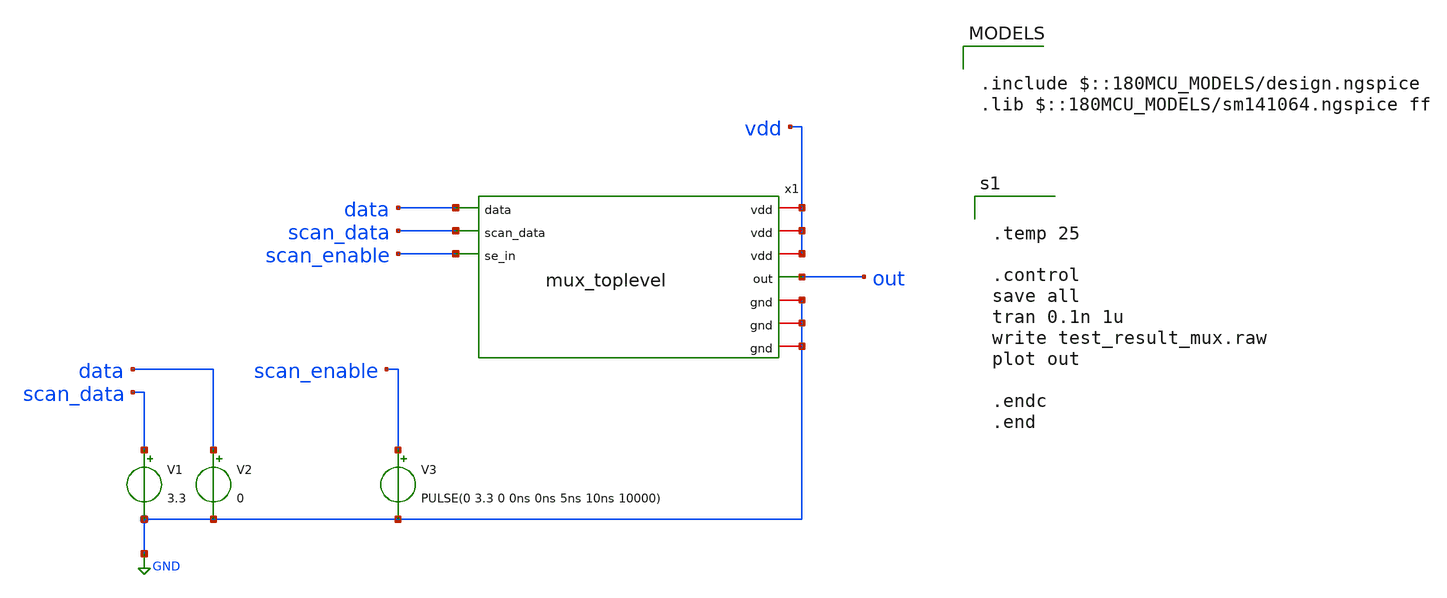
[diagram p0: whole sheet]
** sch_path: designs/schematics/mux2x1_transmission_gate/mux_tb.sch
**.subckt mux_tb
V1 scan_data GND 3.3
V2 data GND 0
V3 scan_enable GND PULSE(0 3.3 0 0ns 0ns 5ns 10ns 10000)
x1 vdd data GND out scan_data scan_enable mux_toplevel
**** begin user architecture code

.include $::180MCU_MODELS/design.ngspice
.lib $::180MCU_MODELS/sm141064.ngspice ff



.temp 25

.control
save all
tran 0.1n 1u
write test_result_mux.raw
plot out

.endc
.end


.option
save all

.control
tran 0 1u
.endc
.end
**** end user architecture code
**.ends

* expanding   symbol:  schematics/mux2x1_transmission_gate/mux_toplevel.sym # of pins=10
** sym_path: designs/schematics/mux2x1_transmission_gate/mux_toplevel.sym
** sch_path: designs/schematics/mux2x1_transmission_gate/mux_toplevel.sch
.subckt mux_toplevel vdd data gnd out scan_data se_in
*.iopin vdd
*.iopin gnd
*.opin out
*.ipin data
*.ipin scan_data
*.ipin se_in
*.iopin vdd
*.iopin gnd
*.iopin gnd
*.iopin vdd
x1 vdd se_in net1 gnd mux_ctrl_logic
x2 vdd net1 data out se_in gnd mux_tg
x3 vdd se_in scan_data out net1 gnd mux_tg
.ends


* expanding   symbol:  mux_transmission_gate/mux_ctrl_logic.sym # of pins=4
** sym_path: designs/schematics/mux2x1_transmission_gate/mux_ctrl_logic.sym
** sch_path: designs/schematics/mux2x1_transmission_gate/mux_ctrl_logic.sch
.subckt mux_ctrl_logic vdd in out_inv gnd
*.iopin vdd
*.iopin gnd
*.iopin out_inv
*.iopin in
XM1 out_inv in gnd gnd nfet_03v3 L=0.28u W=0.22u nf=1 ad='int((nf+1)/2) * W/nf * 0.18u' as='int((nf+2)/2) * W/nf * 0.18u'
+ pd='2*int((nf+1)/2) * (W/nf + 0.18u)' ps='2*int((nf+2)/2) * (W/nf + 0.18u)' nrd='0.18u / W' nrs='0.18u / W'
+ sa=0 sb=0 sd=0 m=1
XM2 out_inv in vdd vdd pfet_03v3 L=0.28u W=0.22u nf=1 ad='int((nf+1)/2) * W/nf * 0.18u' as='int((nf+2)/2) * W/nf * 0.18u'
+ pd='2*int((nf+1)/2) * (W/nf + 0.18u)' ps='2*int((nf+2)/2) * (W/nf + 0.18u)' nrd='0.18u / W' nrs='0.18u / W'
+ sa=0 sb=0 sd=0 m=1
.ends


* expanding   symbol:  mux_transmission_gate/mux_tg.sym # of pins=6
** sym_path: designs/schematics/mux2x1_transmission_gate/mux_tg.sym
** sch_path: designs/schematics/mux2x1_transmission_gate/mux_tg.sch
.subckt mux_tg vdd pfet_gate in out nfet_gate gnd
*.iopin vdd
*.iopin gnd
*.iopin out
*.iopin in
*.iopin pfet_gate
*.iopin nfet_gate
XM1 in nfet_gate out gnd nfet_03v3 L=0.28u W=0.22u nf=1 ad='int((nf+1)/2) * W/nf * 0.18u' as='int((nf+2)/2) * W/nf * 0.18u'
+ pd='2*int((nf+1)/2) * (W/nf + 0.18u)' ps='2*int((nf+2)/2) * (W/nf + 0.18u)' nrd='0.18u / W' nrs='0.18u / W'
+ sa=0 sb=0 sd=0 m=1
XM2 in pfet_gate out vdd pfet_03v3 L=0.28u W=0.22u nf=1 ad='int((nf+1)/2) * W/nf * 0.18u' as='int((nf+2)/2) * W/nf * 0.18u'
+ pd='2*int((nf+1)/2) * (W/nf + 0.18u)' ps='2*int((nf+2)/2) * (W/nf + 0.18u)' nrd='0.18u / W' nrs='0.18u / W'
+ sa=0 sb=0 sd=0 m=1
.ends

.GLOBAL GND
.end
